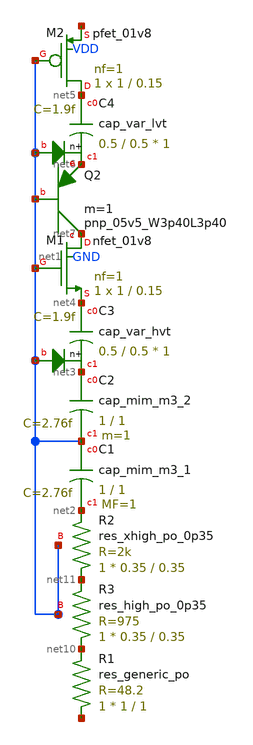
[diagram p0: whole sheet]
** sch_path: xschem/part.sch
**.subckt part
XC1 net1 net2 sky130_fd_pr__cap_mim_m3_1 W=1 L=1 MF=1 m=1
XC2 net3 net1 sky130_fd_pr__cap_mim_m3_2 W=1 L=1 MF=1 m=1
XC3 net4 net3 net1 sky130_fd_pr__cap_var_hvt W=0.5 L=0.5 VM=1 m=1
XC4 net5 net6 net1 sky130_fd_pr__cap_var_lvt W=0.5 L=0.5 VM=1 m=1
XM1 net7 net1 net4 GND sky130_fd_pr__nfet_01v8 L=0.15 W=1 nf=1 ad='int((nf+1)/2) * W/nf * 0.29' as='int((nf+2)/2) * W/nf * 0.29'
+ pd='2*int((nf+1)/2) * (W/nf + 0.29)' ps='2*int((nf+2)/2) * (W/nf + 0.29)' nrd='0.29 / W' nrs='0.29 / W'
+ sa=0 sb=0 sd=0 mult=1 m=1
XM2 net5 net1 net8 VDD sky130_fd_pr__pfet_01v8 L=0.15 W=1 nf=1 ad='int((nf+1)/2) * W/nf * 0.29' as='int((nf+2)/2) * W/nf * 0.29'
+ pd='2*int((nf+1)/2) * (W/nf + 0.29)' ps='2*int((nf+2)/2) * (W/nf + 0.29)' nrd='0.29 / W' nrs='0.29 / W'
+ sa=0 sb=0 sd=0 mult=1 m=1
XQ2 net7 net1 net6 sky130_fd_pr__pnp_05v5_W3p40L3p40 m=1
XR1 net9 net10 sky130_fd_pr__res_generic_po W=1 L=1 m=1
XR2 net11 net2 net1 sky130_fd_pr__res_xhigh_po_0p35 L=0.35 mult=1 m=1
XR3 net10 net11 net1 sky130_fd_pr__res_high_po_0p35 L=0.35 mult=1 m=1
**.ends
.end
